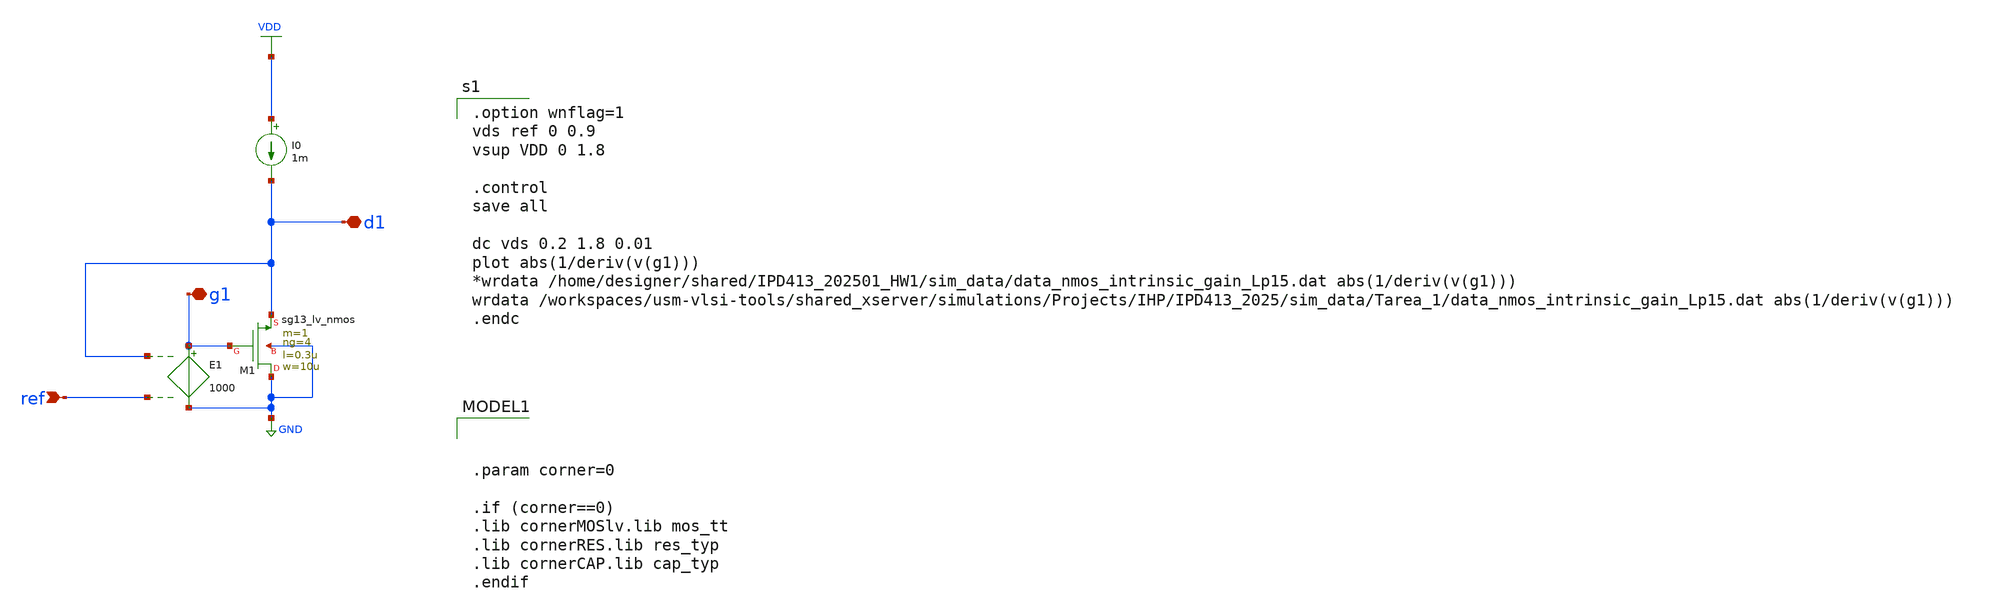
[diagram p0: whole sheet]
** sch_path: xschem/Tareas/Tarea_1/nmoslv_instrinsic_gain_IPD413-202501-HW1.sch
**.subckt nmoslv_instrinsic_gain_IPD413-202501-HW1 ref g1 d1
*.ipin ref
*.iopin g1
*.iopin d1
E1 g1 GND d1 ref 1000
I0 VDD d1 1m
XM1 GND g1 d1 GND sg13_lv_nmos w=10u l=0.3u ng=4 m=1 mm_ok=1
**** begin user architecture code

.option wnflag=1
vds ref 0 0.9
vsup VDD 0 1.8

.control
save all

dc vds 0.2 1.8 0.01
plot abs(1/deriv(v(g1)))
*wrdata /home/designer/shared/IPD413_202501_HW1/sim_data/data_nmos_intrinsic_gain_Lp15.dat
*+ abs(1/deriv(v(g1)))
wrdata
+ /workspaces/usm-vlsi-tools/shared_xserver/simulations/Projects/IHP/IPD413_2025/sim_data/Tarea_1/data_nmos_intrinsic_gain_Lp15.dat abs(1/deriv(v(g1)))
.endc



.param corner=0

.if (corner==0)
.lib cornerMOSlv.lib mos_tt
.lib cornerRES.lib res_typ
.lib cornerCAP.lib cap_typ
.endif

**** end user architecture code
**.ends
.GLOBAL GND
.GLOBAL VDD
.end
